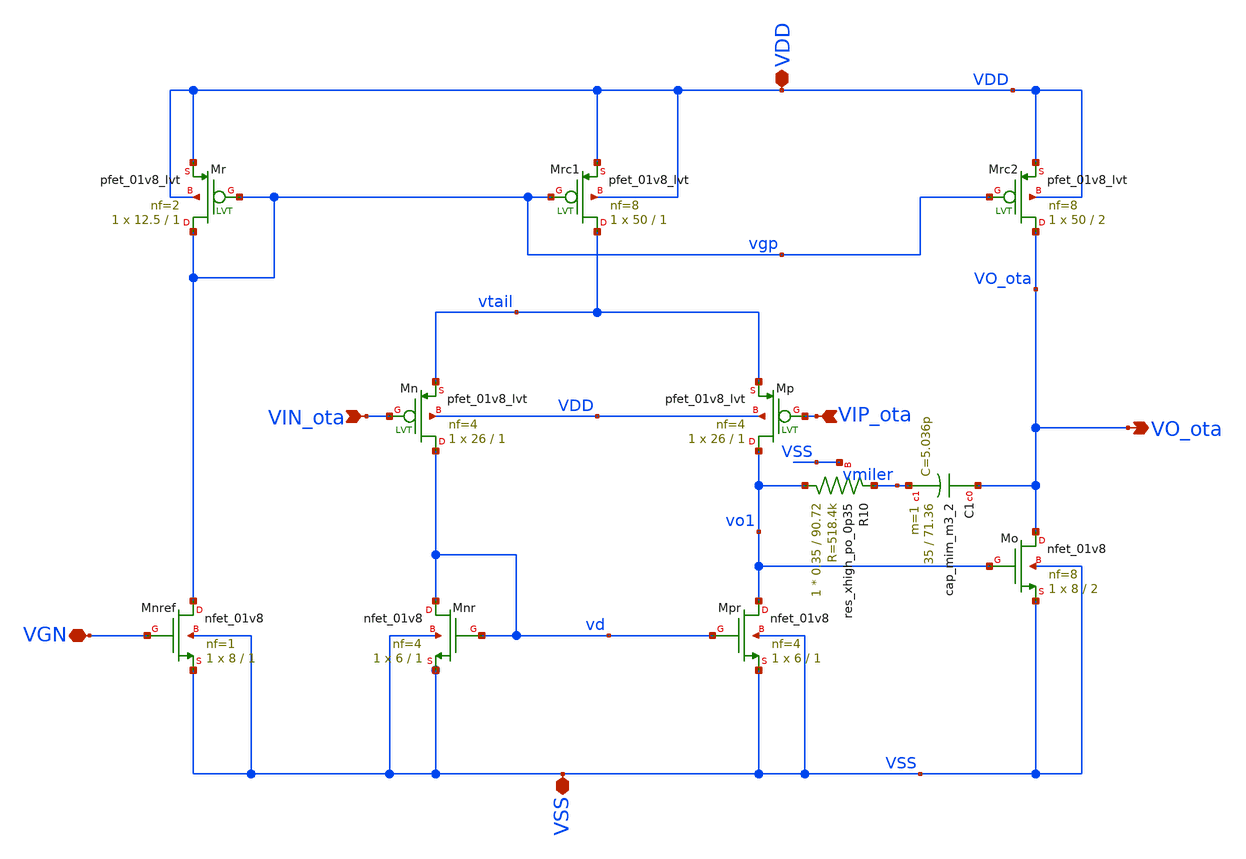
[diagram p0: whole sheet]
** sch_path: xschem/OTA/OTA.sch
**.subckt OTA VIN_ota VO_ota VSS VDD VIP_ota VGN
*.ipin VIN_ota
*.opin VO_ota
*.iopin VSS
*.iopin VDD
*.ipin VIP_ota
*.iopin VGN
XMpr vo1 vd VSS VSS sky130_fd_pr__nfet_01v8 L=1 W=6 nf=4 ad='int((4 + 1)/2) * 6 / 4 * 0.29' as='int((4 + 2)/2) * 6 / 4 * 0.29'
+ pd='2*int((4 + 1)/2) * (6 / 4 + 0.29)' ps='2*int((4 + 2)/2) * (6 / 4 + 0.29)' nrd='0.29 / 6 ' nrs='0.29 / 6 '
+ sa=0 sb=0 sd=0 mult=1 m=1
XMnr vd vd VSS VSS sky130_fd_pr__nfet_01v8 L=1 W=6 nf=4 ad='int((4 + 1)/2) * 6 / 4 * 0.29' as='int((4 + 2)/2) * 6 / 4 * 0.29'
+ pd='2*int((4 + 1)/2) * (6 / 4 + 0.29)' ps='2*int((4 + 2)/2) * (6 / 4 + 0.29)' nrd='0.29 / 6 ' nrs='0.29 / 6 '
+ sa=0 sb=0 sd=0 mult=1 m=1
XMo VO_ota vo1 VSS VSS sky130_fd_pr__nfet_01v8 L=2 W=8 nf=8 ad='int((8 + 1)/2) * 8 / 8 * 0.29' as='int((8 + 2)/2) * 8 / 8 * 0.29'
+ pd='2*int((8 + 1)/2) * (8 / 8 + 0.29)' ps='2*int((8 + 2)/2) * (8 / 8 + 0.29)' nrd='0.29 / 8 ' nrs='0.29 / 8 '
+ sa=0 sb=0 sd=0 mult=1 m=1
XMrc2 VO_ota vgp VDD VDD sky130_fd_pr__pfet_01v8_lvt L=2 W=50 nf=8 ad='int((8 + 1)/2) * 50 / 8 * 0.29'
+ as='int((8 + 2)/2) * 50 / 8 * 0.29' pd='2*int((8 + 1)/2) * (50 / 8 + 0.29)' ps='2*int((8 + 2)/2) * (50 / 8 + 0.29)'
+ nrd='0.29 / 50 ' nrs='0.29 / 50 ' sa=0 sb=0 sd=0 mult=1 m=1
XC1 VO_ota vmiler sky130_fd_pr__cap_mim_m3_2 W=35 L=71.36 MF=1 m=1
XMp vo1 VIP_ota vtail VDD sky130_fd_pr__pfet_01v8_lvt L=1 W=26 nf=4 ad='int((4 + 1)/2) * 26 / 4 * 0.29'
+ as='int((4 + 2)/2) * 26 / 4 * 0.29' pd='2*int((4 + 1)/2) * (26 / 4 + 0.29)' ps='2*int((4 + 2)/2) * (26 / 4 + 0.29)'
+ nrd='0.29 / 26 ' nrs='0.29 / 26 ' sa=0 sb=0 sd=0 mult=1 m=1
XMn vd VIN_ota vtail VDD sky130_fd_pr__pfet_01v8_lvt L=1 W=26 nf=4 ad='int((4 + 1)/2) * 26 / 4 * 0.29'
+ as='int((4 + 2)/2) * 26 / 4 * 0.29' pd='2*int((4 + 1)/2) * (26 / 4 + 0.29)' ps='2*int((4 + 2)/2) * (26 / 4 + 0.29)'
+ nrd='0.29 / 26 ' nrs='0.29 / 26 ' sa=0 sb=0 sd=0 mult=1 m=1
XMrc1 vtail vgp VDD VDD sky130_fd_pr__pfet_01v8_lvt L=1 W=50 nf=8 ad='int((8 + 1)/2) * 50 / 8 * 0.29'
+ as='int((8 + 2)/2) * 50 / 8 * 0.29' pd='2*int((8 + 1)/2) * (50 / 8 + 0.29)' ps='2*int((8 + 2)/2) * (50 / 8 + 0.29)'
+ nrd='0.29 / 50 ' nrs='0.29 / 50 ' sa=0 sb=0 sd=0 mult=1 m=1
XMr vgp vgp VDD VDD sky130_fd_pr__pfet_01v8_lvt L=1 W=12.5 nf=2 ad='int((2 + 1)/2) * 12.5 / 2 * 0.29'
+ as='int((2 + 2)/2) * 12.5 / 2 * 0.29' pd='2*int((2 + 1)/2) * (12.5 / 2 + 0.29)' ps='2*int((2 + 2)/2) * (12.5 / 2 + 0.29)'
+ nrd='0.29 / 12.5 ' nrs='0.29 / 12.5 ' sa=0 sb=0 sd=0 mult=1 m=1
XMnref vgp VGN VSS VSS sky130_fd_pr__nfet_01v8 L=1 W=8 nf=1 ad='int((1 + 1)/2) * 8 / 1 * 0.29' as='int((1 + 2)/2) * 8 / 1 * 0.29'
+ pd='2*int((1 + 1)/2) * (8 / 1 + 0.29)' ps='2*int((1 + 2)/2) * (8 / 1 + 0.29)' nrd='0.29 / 8 ' nrs='0.29 / 8 '
+ sa=0 sb=0 sd=0 mult=1 m=1
XR10 vo1 vmiler VSS sky130_fd_pr__res_xhigh_po_0p35 L=90.72 mult=1 m=1
**.ends
.end
